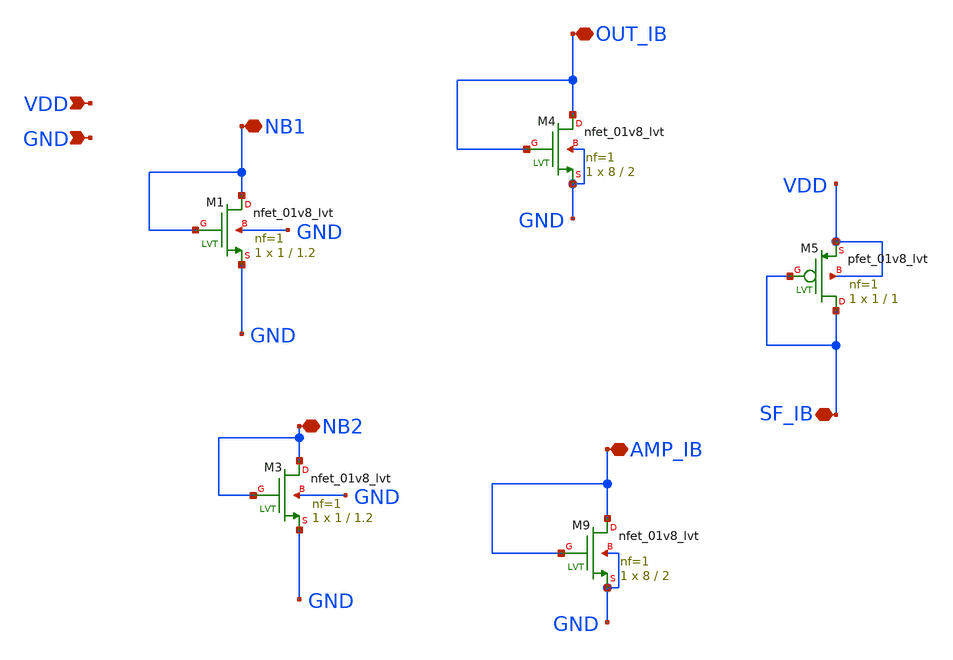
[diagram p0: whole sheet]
** sch_path: xschem/biases.sch
**.subckt biases VDD GND NB1 NB2 OUT_IB AMP_IB SF_IB
*.ipin VDD
*.ipin GND
*.iopin NB1
*.iopin NB2
*.iopin OUT_IB
*.iopin AMP_IB
*.iopin SF_IB
XM1 NB1 NB1 GND GND sky130_fd_pr__nfet_01v8_lvt L=1.2 W=1 nf=1 ad='int((nf+1)/2) * W/nf * 0.29' as='int((nf+2)/2) * W/nf * 0.29'
+ pd='2*int((nf+1)/2) * (W/nf + 0.29)' ps='2*int((nf+2)/2) * (W/nf + 0.29)' nrd='0.29 / W' nrs='0.29 / W'
+ sa=0 sb=0 sd=0 mult=1 m=1
XM3 NB2 NB2 GND GND sky130_fd_pr__nfet_01v8_lvt L=1.2 W=1 nf=1 ad='int((nf+1)/2) * W/nf * 0.29' as='int((nf+2)/2) * W/nf * 0.29'
+ pd='2*int((nf+1)/2) * (W/nf + 0.29)' ps='2*int((nf+2)/2) * (W/nf + 0.29)' nrd='0.29 / W' nrs='0.29 / W'
+ sa=0 sb=0 sd=0 mult=1 m=1
XM5 SF_IB SF_IB VDD VDD sky130_fd_pr__pfet_01v8_lvt L=1 W=1 nf=1 ad='int((nf+1)/2) * W/nf * 0.29' as='int((nf+2)/2) * W/nf * 0.29'
+ pd='2*int((nf+1)/2) * (W/nf + 0.29)' ps='2*int((nf+2)/2) * (W/nf + 0.29)' nrd='0.29 / W' nrs='0.29 / W'
+ sa=0 sb=0 sd=0 mult=1 m=1
XM4 OUT_IB OUT_IB GND GND sky130_fd_pr__nfet_01v8_lvt L=2 W=8 nf=1 ad='int((nf+1)/2) * W/nf * 0.29' as='int((nf+2)/2) * W/nf * 0.29'
+ pd='2*int((nf+1)/2) * (W/nf + 0.29)' ps='2*int((nf+2)/2) * (W/nf + 0.29)' nrd='0.29 / W' nrs='0.29 / W'
+ sa=0 sb=0 sd=0 mult=1 m=1
XM9 AMP_IB AMP_IB GND GND sky130_fd_pr__nfet_01v8_lvt L=2 W=8 nf=1 ad='int((nf+1)/2) * W/nf * 0.29' as='int((nf+2)/2) * W/nf * 0.29'
+ pd='2*int((nf+1)/2) * (W/nf + 0.29)' ps='2*int((nf+2)/2) * (W/nf + 0.29)' nrd='0.29 / W' nrs='0.29 / W'
+ sa=0 sb=0 sd=0 mult=1 m=1
**.ends
.end
